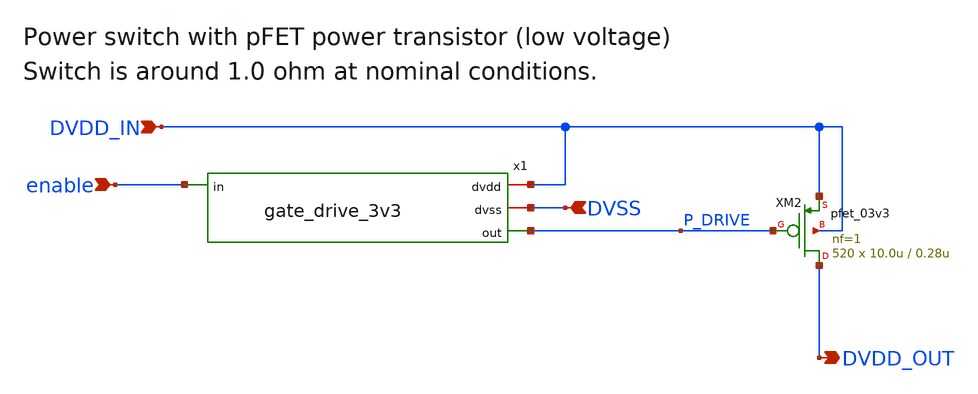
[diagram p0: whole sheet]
** sch_path: xschem/power_stage3v3.sch
**.subckt power_stage3v3 enable DVDD_IN DVSS DVDD_OUT
*.ipin enable
*.ipin DVDD_IN
*.ipin DVSS
*.opin DVDD_OUT
XM2 DVDD_OUT P_DRIVE DVDD_IN DVDD_IN pfet_03v3 L=0.28u W=10.0u nf=1 ad='int((nf+1)/2) * W/nf * 0.18u'
+ as='int((nf+2)/2) * W/nf * 0.18u' pd='2*int((nf+1)/2) * (W/nf + 0.18u)' ps='2*int((nf+2)/2) * (W/nf + 0.18u)'
+ nrd='0.18u / W' nrs='0.18u / W' sa=0 sb=0 sd=0 m=520 par=520
x1 DVDD_IN DVSS P_DRIVE enable gate_drive_3v3
**.ends
.end
